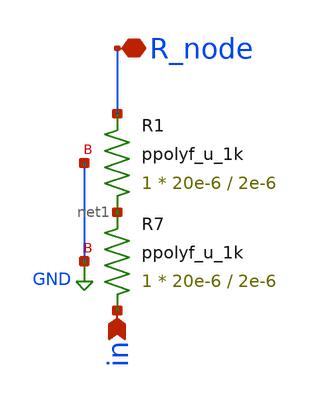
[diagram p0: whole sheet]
** sch_path: xschem/dac_sub_therm.sch
**.subckt dac_sub_therm in R_node
*.ipin in
*.iopin R_node
XR7 in net1 GND ppolyf_u_1k r_width=20e-6 r_length=2e-6 m=1
XR1 net1 R_node GND ppolyf_u_1k r_width=20e-6 r_length=2e-6 m=1
**.ends
.GLOBAL GND
.end
